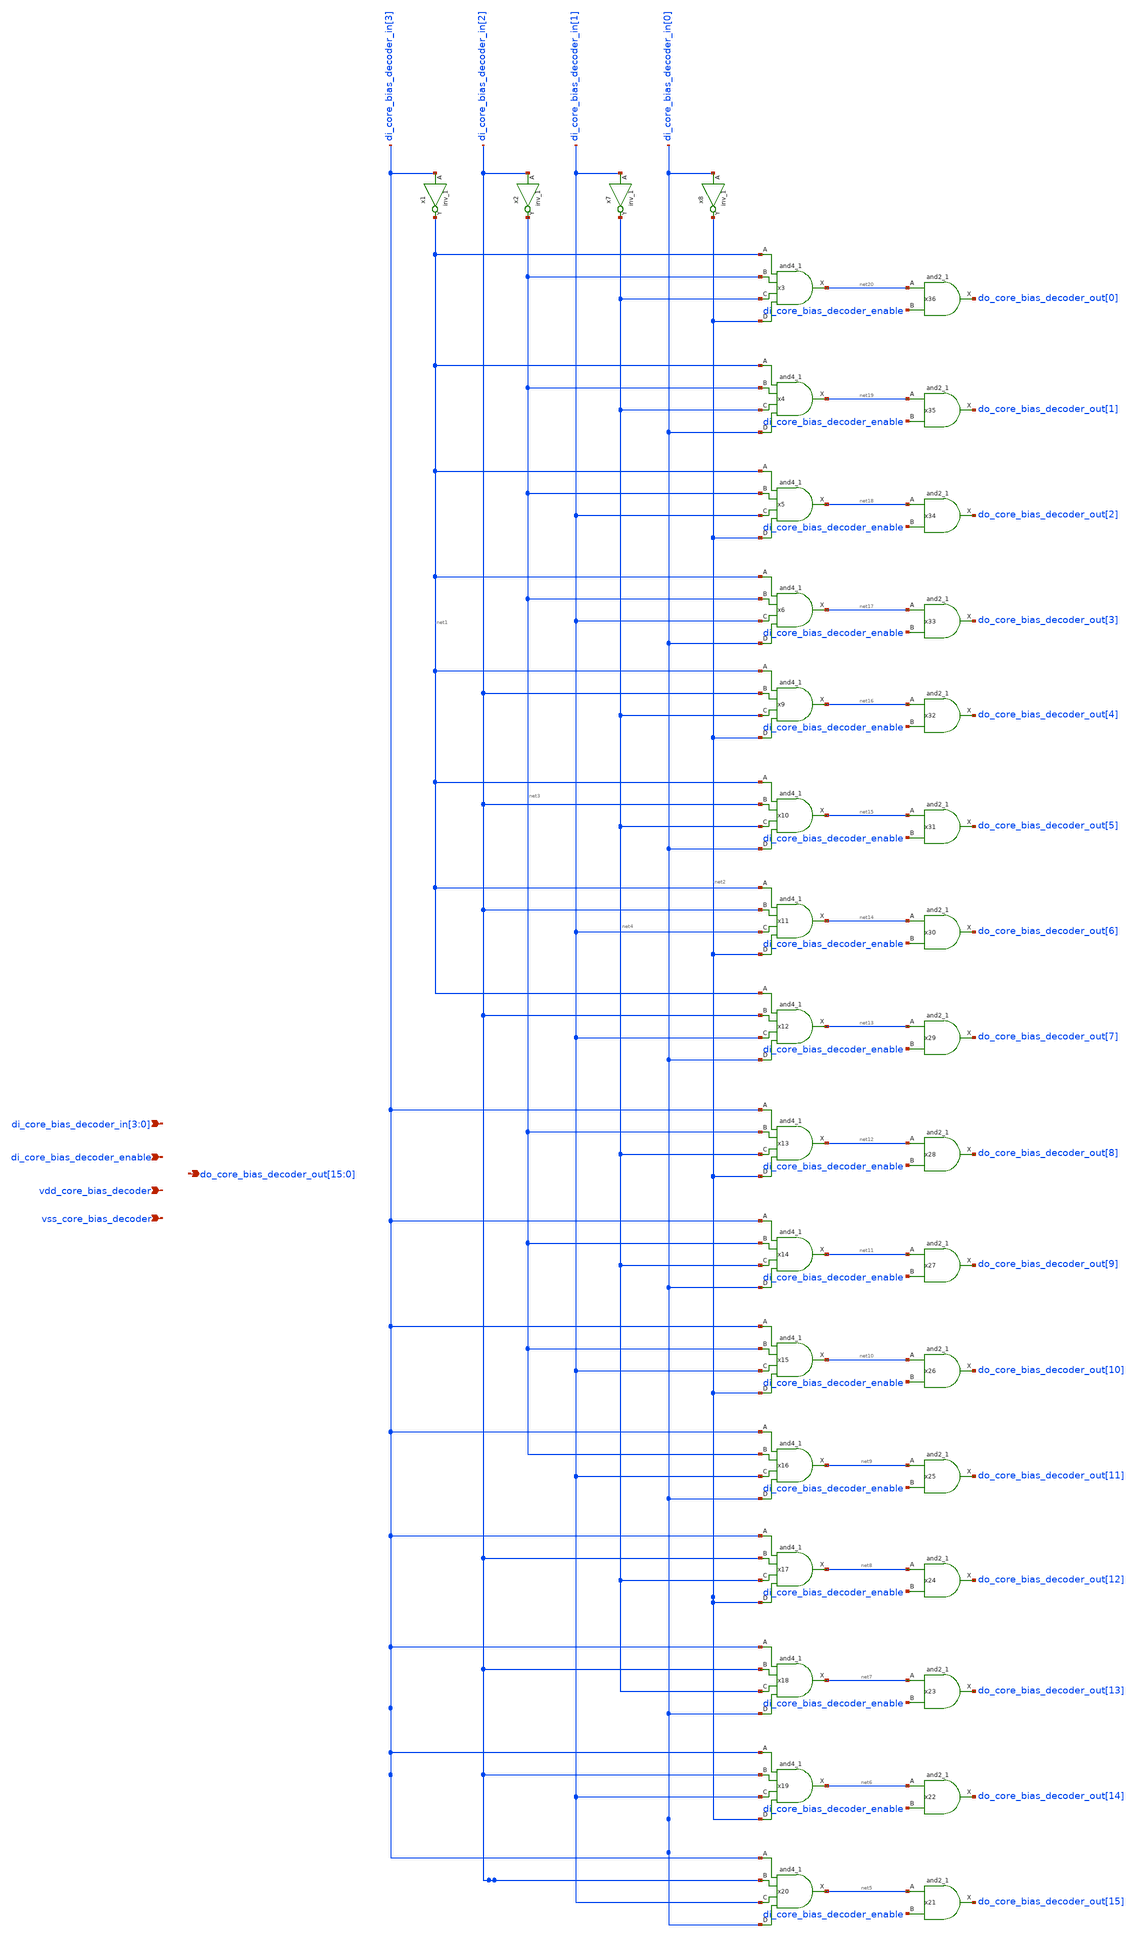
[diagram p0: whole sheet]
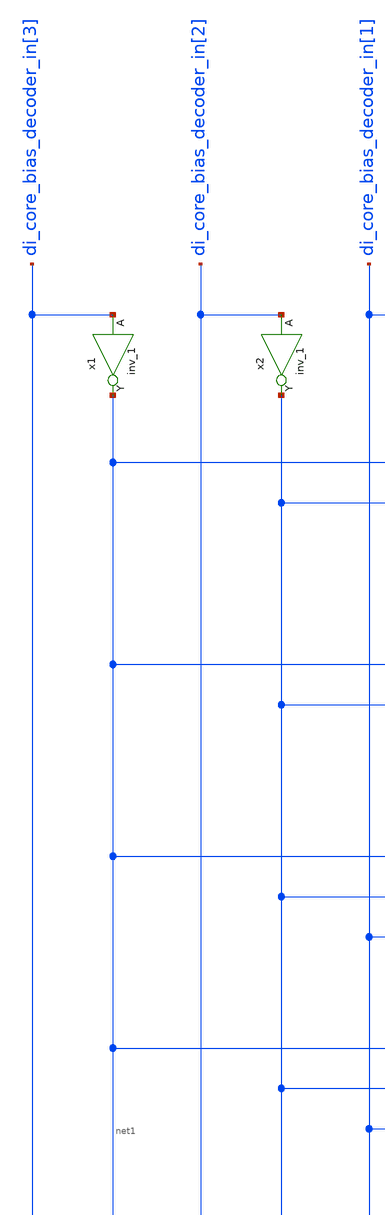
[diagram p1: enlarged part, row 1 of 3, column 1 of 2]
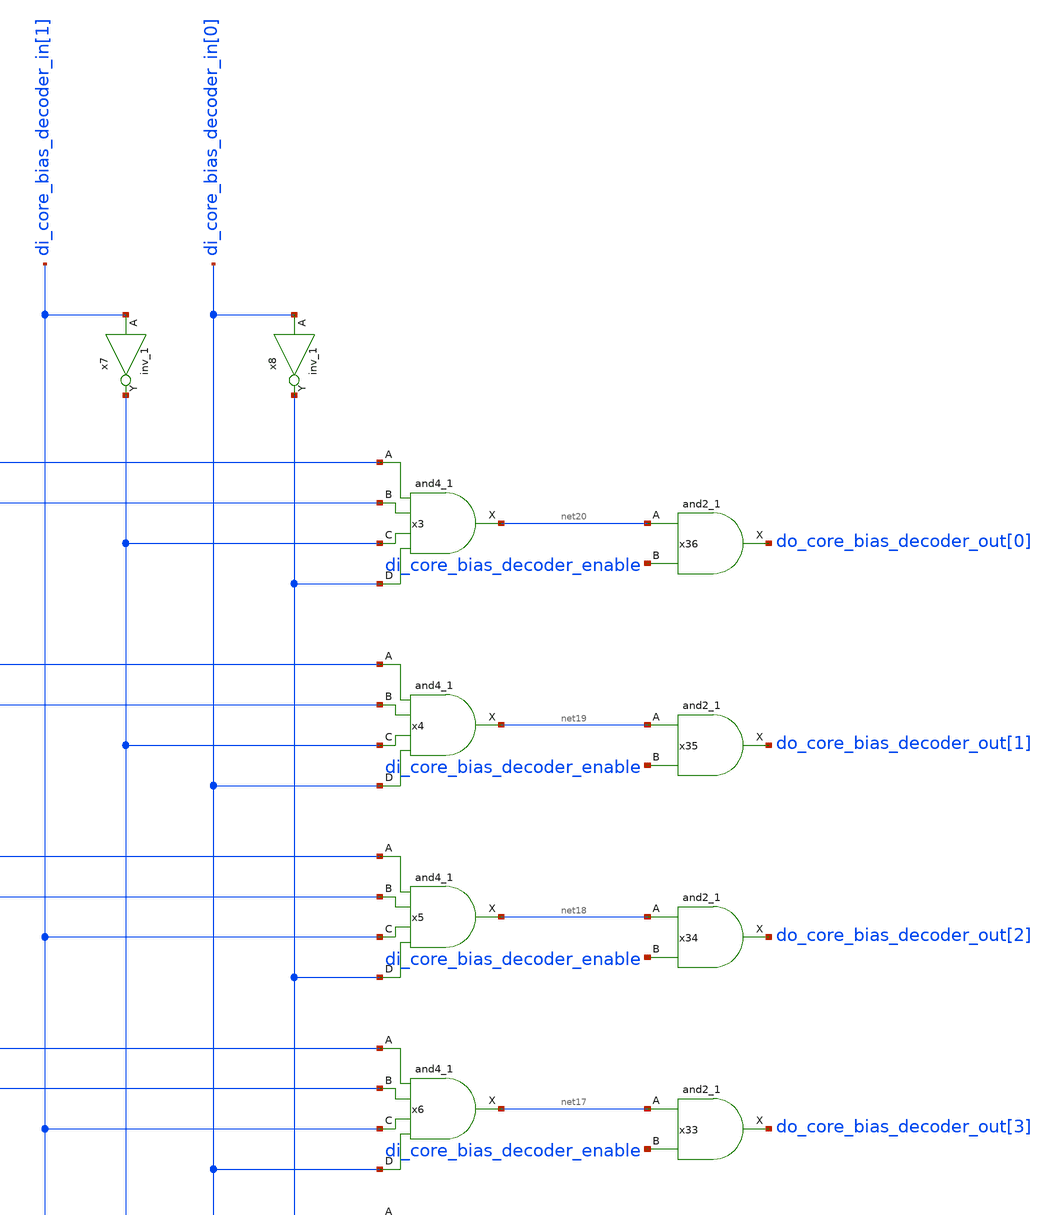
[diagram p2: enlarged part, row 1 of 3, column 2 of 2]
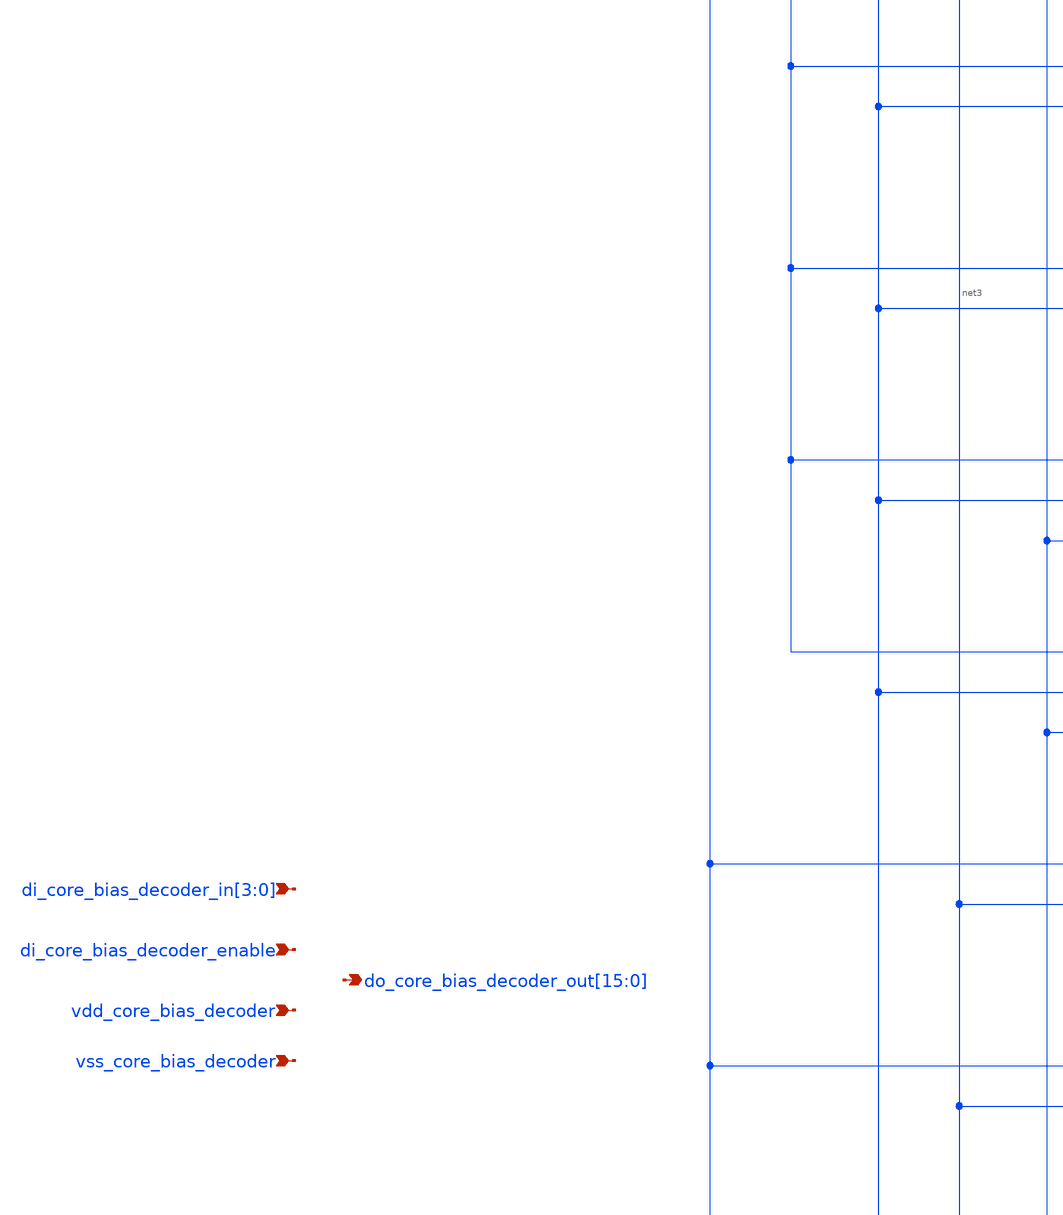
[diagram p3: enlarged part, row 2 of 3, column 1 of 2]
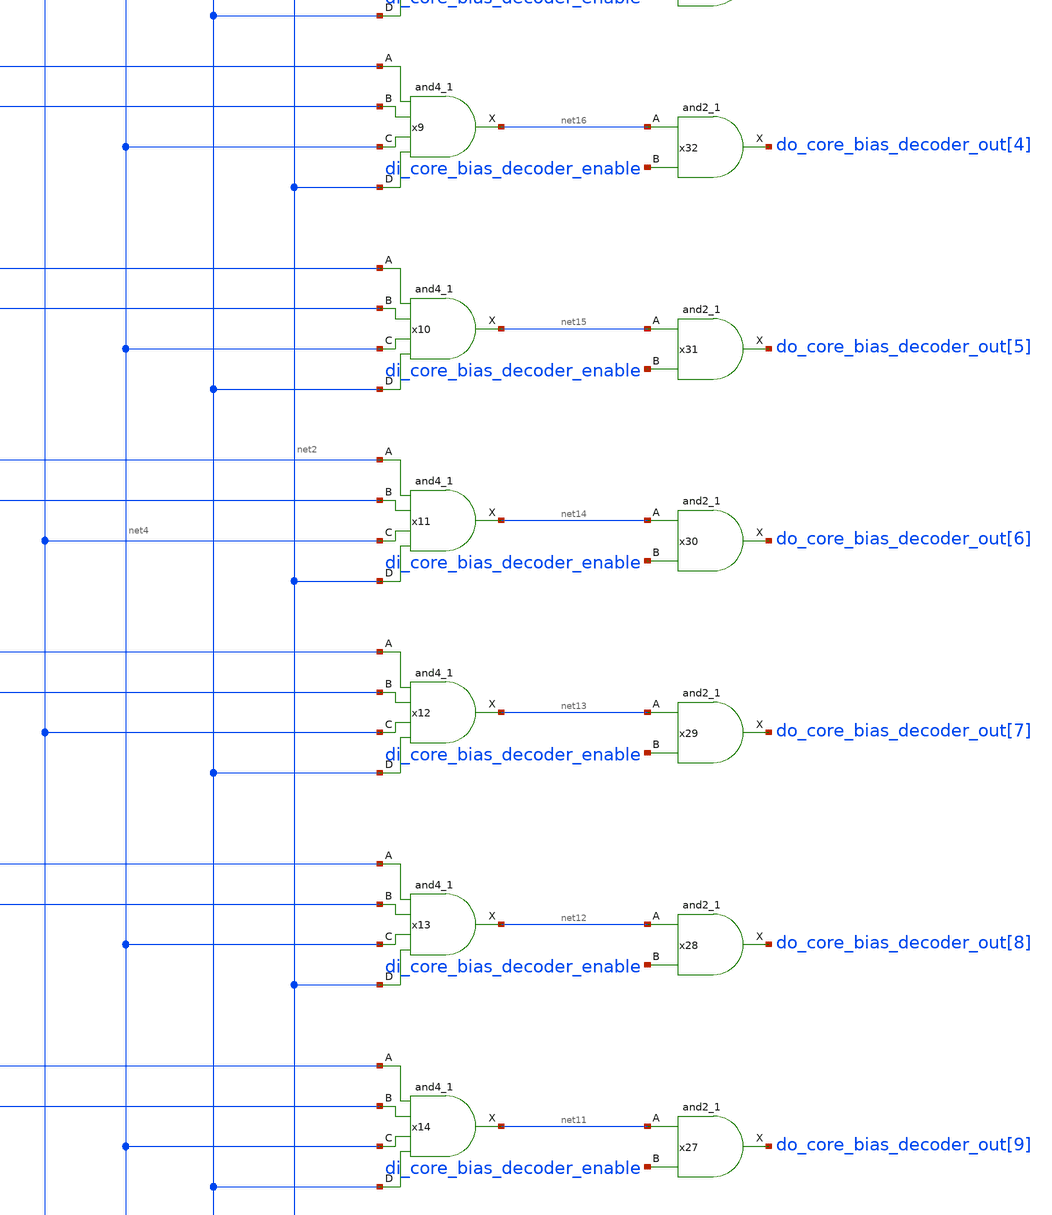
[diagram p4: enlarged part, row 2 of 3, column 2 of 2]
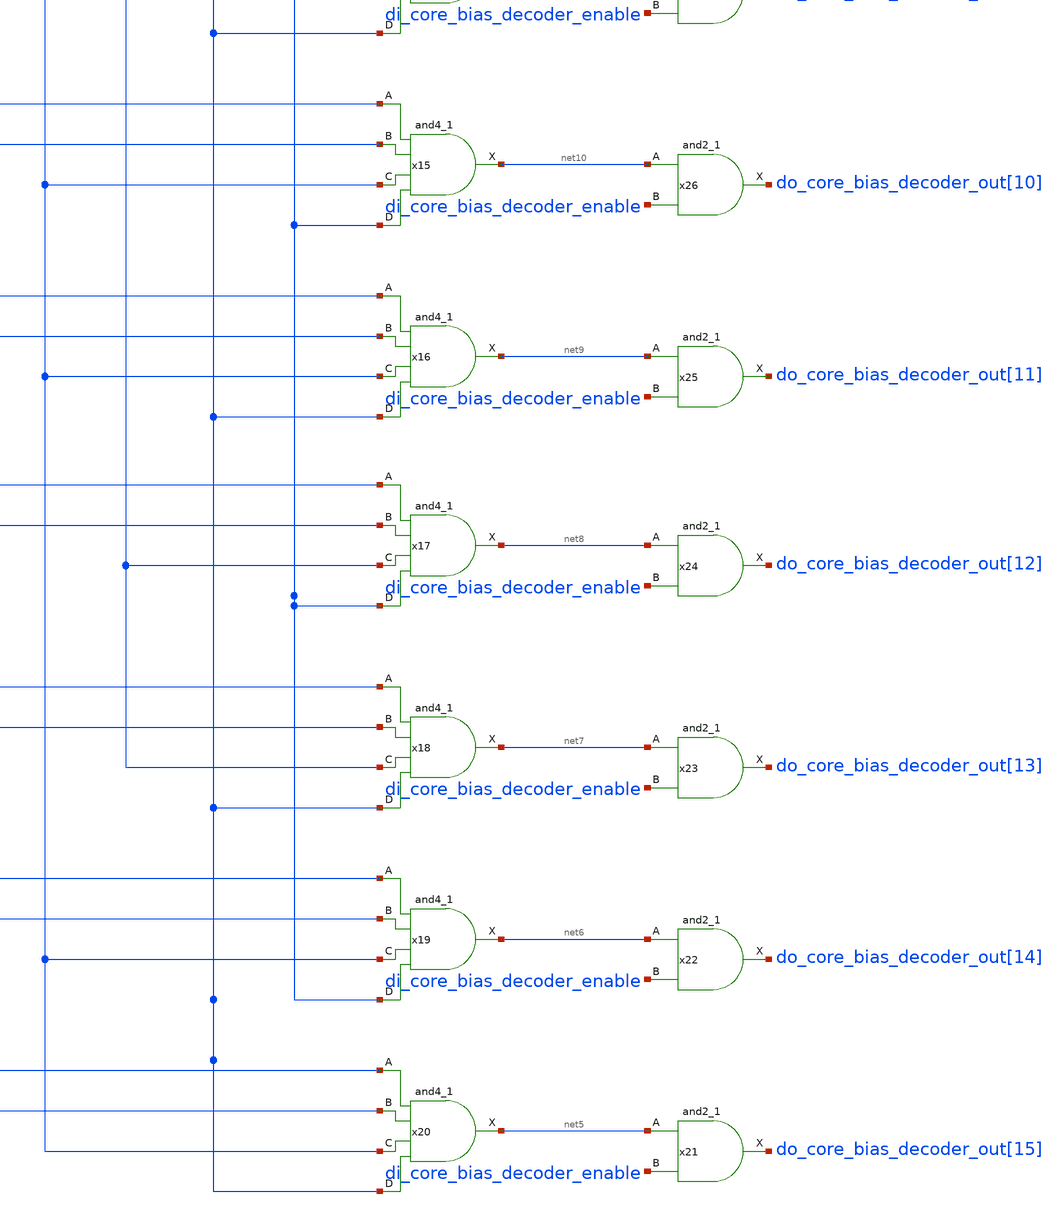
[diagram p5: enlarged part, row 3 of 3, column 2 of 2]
** sch_path: lna_core_bias_res_decoder.sch
**.subckt lna_core_bias_res_decoder
*+ do_core_bias_decoder_out[15],do_core_bias_decoder_out[14],do_core_bias_decoder_out[13],do_core_bias_decoder_out[12],do_core_bias_decoder_out[11],do_core_bias_decoder_out[10],do_core_bias_decoder_out[9],do_core_bias_decoder_out[8],do_core_bias_decoder_out[7],do_core_bias_decoder_out[6],do_core_bias_decoder_out[5],do_core_bias_decoder_out[4],do_core_bias_decoder_out[3],do_core_bias_decoder_out[2],do_core_bias_decoder_out[1],do_core_bias_decoder_out[0]
*+ di_core_bias_decoder_in[3],di_core_bias_decoder_in[2],di_core_bias_decoder_in[1],di_core_bias_decoder_in[0] di_core_bias_decoder_enable vdd_core_bias_decoder vss_core_bias_decoder
*.opin
*+ do_core_bias_decoder_out[15],do_core_bias_decoder_out[14],do_core_bias_decoder_out[13],do_core_bias_decoder_out[12],do_core_bias_decoder_out[11],do_core_bias_decoder_out[10],do_core_bias_decoder_out[9],do_core_bias_decoder_out[8],do_core_bias_decoder_out[7],do_core_bias_decoder_out[6],do_core_bias_decoder_out[5],do_core_bias_decoder_out[4],do_core_bias_decoder_out[3],do_core_bias_decoder_out[2],do_core_bias_decoder_out[1],do_core_bias_decoder_out[0]
*.ipin
*+ di_core_bias_decoder_in[3],di_core_bias_decoder_in[2],di_core_bias_decoder_in[1],di_core_bias_decoder_in[0]
*.ipin di_core_bias_decoder_enable
*.ipin vdd_core_bias_decoder
*.ipin vss_core_bias_decoder
x1 di_core_bias_decoder_in[3] vss_core_bias_decoder vss_core_bias_decoder vdd_core_bias_decoder
+ vdd_core_bias_decoder net1 sky130_fd_sc_hd__inv_1
x2 di_core_bias_decoder_in[2] vss_core_bias_decoder vss_core_bias_decoder vdd_core_bias_decoder
+ vdd_core_bias_decoder net3 sky130_fd_sc_hd__inv_1
x7 di_core_bias_decoder_in[1] vss_core_bias_decoder vss_core_bias_decoder vdd_core_bias_decoder
+ vdd_core_bias_decoder net4 sky130_fd_sc_hd__inv_1
x8 di_core_bias_decoder_in[0] vss_core_bias_decoder vss_core_bias_decoder vdd_core_bias_decoder
+ vdd_core_bias_decoder net2 sky130_fd_sc_hd__inv_1
x3 net1 net3 net4 net2 vss_core_bias_decoder vss_core_bias_decoder vdd_core_bias_decoder
+ vdd_core_bias_decoder net20 sky130_fd_sc_hd__and4_1
x4 net1 net3 net4 di_core_bias_decoder_in[0] vss_core_bias_decoder vss_core_bias_decoder
+ vdd_core_bias_decoder vdd_core_bias_decoder net19 sky130_fd_sc_hd__and4_1
x5 net1 net3 di_core_bias_decoder_in[1] net2 vss_core_bias_decoder vss_core_bias_decoder
+ vdd_core_bias_decoder vdd_core_bias_decoder net18 sky130_fd_sc_hd__and4_1
x6 net1 net3 di_core_bias_decoder_in[1] di_core_bias_decoder_in[0] vss_core_bias_decoder
+ vss_core_bias_decoder vdd_core_bias_decoder vdd_core_bias_decoder net17 sky130_fd_sc_hd__and4_1
x9 net1 di_core_bias_decoder_in[2] net4 net2 vss_core_bias_decoder vss_core_bias_decoder
+ vdd_core_bias_decoder vdd_core_bias_decoder net16 sky130_fd_sc_hd__and4_1
x10 net1 di_core_bias_decoder_in[2] net4 di_core_bias_decoder_in[0] vss_core_bias_decoder
+ vss_core_bias_decoder vdd_core_bias_decoder vdd_core_bias_decoder net15 sky130_fd_sc_hd__and4_1
x11 net1 di_core_bias_decoder_in[2] di_core_bias_decoder_in[1] net2 vss_core_bias_decoder
+ vss_core_bias_decoder vdd_core_bias_decoder vdd_core_bias_decoder net14 sky130_fd_sc_hd__and4_1
x12 net1 di_core_bias_decoder_in[2] di_core_bias_decoder_in[1] di_core_bias_decoder_in[0]
+ vss_core_bias_decoder vss_core_bias_decoder vdd_core_bias_decoder vdd_core_bias_decoder net13 sky130_fd_sc_hd__and4_1
x13 di_core_bias_decoder_in[3] net3 net4 net2 vss_core_bias_decoder vss_core_bias_decoder
+ vdd_core_bias_decoder vdd_core_bias_decoder net12 sky130_fd_sc_hd__and4_1
x14 di_core_bias_decoder_in[3] net3 net4 di_core_bias_decoder_in[0] vss_core_bias_decoder
+ vss_core_bias_decoder vdd_core_bias_decoder vdd_core_bias_decoder net11 sky130_fd_sc_hd__and4_1
x15 di_core_bias_decoder_in[3] net3 di_core_bias_decoder_in[1] net2 vss_core_bias_decoder
+ vss_core_bias_decoder vdd_core_bias_decoder vdd_core_bias_decoder net10 sky130_fd_sc_hd__and4_1
x16 di_core_bias_decoder_in[3] net3 di_core_bias_decoder_in[1] di_core_bias_decoder_in[0]
+ vss_core_bias_decoder vss_core_bias_decoder vdd_core_bias_decoder vdd_core_bias_decoder net9 sky130_fd_sc_hd__and4_1
x17 di_core_bias_decoder_in[3] di_core_bias_decoder_in[2] net4 net2 vss_core_bias_decoder
+ vss_core_bias_decoder vdd_core_bias_decoder vdd_core_bias_decoder net8 sky130_fd_sc_hd__and4_1
x18 di_core_bias_decoder_in[3] di_core_bias_decoder_in[2] net4 di_core_bias_decoder_in[0]
+ vss_core_bias_decoder vss_core_bias_decoder vdd_core_bias_decoder vdd_core_bias_decoder net7 sky130_fd_sc_hd__and4_1
x19 di_core_bias_decoder_in[3] di_core_bias_decoder_in[2] di_core_bias_decoder_in[1] net2
+ vss_core_bias_decoder vss_core_bias_decoder vdd_core_bias_decoder vdd_core_bias_decoder net6 sky130_fd_sc_hd__and4_1
x20 di_core_bias_decoder_in[3] di_core_bias_decoder_in[2] di_core_bias_decoder_in[1]
+ di_core_bias_decoder_in[0] vss_core_bias_decoder vss_core_bias_decoder vdd_core_bias_decoder vdd_core_bias_decoder net5
+ sky130_fd_sc_hd__and4_1
x21 net5 di_core_bias_decoder_enable vss_core_bias_decoder vss_core_bias_decoder
+ vdd_core_bias_decoder vdd_core_bias_decoder do_core_bias_decoder_out[15] sky130_fd_sc_hd__and2_1
x22 net6 di_core_bias_decoder_enable vss_core_bias_decoder vss_core_bias_decoder
+ vdd_core_bias_decoder vdd_core_bias_decoder do_core_bias_decoder_out[14] sky130_fd_sc_hd__and2_1
x23 net7 di_core_bias_decoder_enable vss_core_bias_decoder vss_core_bias_decoder
+ vdd_core_bias_decoder vdd_core_bias_decoder do_core_bias_decoder_out[13] sky130_fd_sc_hd__and2_1
x24 net8 di_core_bias_decoder_enable vss_core_bias_decoder vss_core_bias_decoder
+ vdd_core_bias_decoder vdd_core_bias_decoder do_core_bias_decoder_out[12] sky130_fd_sc_hd__and2_1
x25 net9 di_core_bias_decoder_enable vss_core_bias_decoder vss_core_bias_decoder
+ vdd_core_bias_decoder vdd_core_bias_decoder do_core_bias_decoder_out[11] sky130_fd_sc_hd__and2_1
x26 net10 di_core_bias_decoder_enable vss_core_bias_decoder vss_core_bias_decoder
+ vdd_core_bias_decoder vdd_core_bias_decoder do_core_bias_decoder_out[10] sky130_fd_sc_hd__and2_1
x27 net11 di_core_bias_decoder_enable vss_core_bias_decoder vss_core_bias_decoder
+ vdd_core_bias_decoder vdd_core_bias_decoder do_core_bias_decoder_out[9] sky130_fd_sc_hd__and2_1
x28 net12 di_core_bias_decoder_enable vss_core_bias_decoder vss_core_bias_decoder
+ vdd_core_bias_decoder vdd_core_bias_decoder do_core_bias_decoder_out[8] sky130_fd_sc_hd__and2_1
x29 net13 di_core_bias_decoder_enable vss_core_bias_decoder vss_core_bias_decoder
+ vdd_core_bias_decoder vdd_core_bias_decoder do_core_bias_decoder_out[7] sky130_fd_sc_hd__and2_1
x30 net14 di_core_bias_decoder_enable vss_core_bias_decoder vss_core_bias_decoder
+ vdd_core_bias_decoder vdd_core_bias_decoder do_core_bias_decoder_out[6] sky130_fd_sc_hd__and2_1
x31 net15 di_core_bias_decoder_enable vss_core_bias_decoder vss_core_bias_decoder
+ vdd_core_bias_decoder vdd_core_bias_decoder do_core_bias_decoder_out[5] sky130_fd_sc_hd__and2_1
x32 net16 di_core_bias_decoder_enable vss_core_bias_decoder vss_core_bias_decoder
+ vdd_core_bias_decoder vdd_core_bias_decoder do_core_bias_decoder_out[4] sky130_fd_sc_hd__and2_1
x33 net17 di_core_bias_decoder_enable vss_core_bias_decoder vss_core_bias_decoder
+ vdd_core_bias_decoder vdd_core_bias_decoder do_core_bias_decoder_out[3] sky130_fd_sc_hd__and2_1
x34 net18 di_core_bias_decoder_enable vss_core_bias_decoder vss_core_bias_decoder
+ vdd_core_bias_decoder vdd_core_bias_decoder do_core_bias_decoder_out[2] sky130_fd_sc_hd__and2_1
x35 net19 di_core_bias_decoder_enable vss_core_bias_decoder vss_core_bias_decoder
+ vdd_core_bias_decoder vdd_core_bias_decoder do_core_bias_decoder_out[1] sky130_fd_sc_hd__and2_1
x36 net20 di_core_bias_decoder_enable vss_core_bias_decoder vss_core_bias_decoder
+ vdd_core_bias_decoder vdd_core_bias_decoder do_core_bias_decoder_out[0] sky130_fd_sc_hd__and2_1
**.ends
.end
